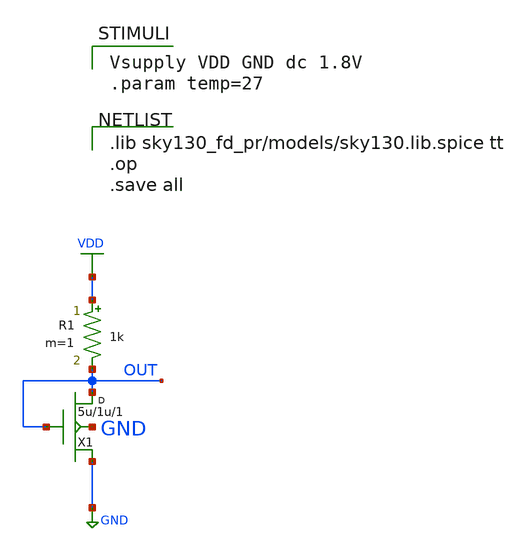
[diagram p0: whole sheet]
** sch_path: tool-test/tooltest.sch
**.subckt tooltest
X1 OUT OUT GND GND sky130_fd_pr__nfet_01v8 w=5u l=1u m=1
R1 VDD OUT 1k m=1
**** begin user architecture code

.lib sky130_fd_pr/models/sky130.lib.spice tt
.op
.save all


Vsupply VDD GND dc 1.8V
.param temp=27

**** end user architecture code
**.ends
.GLOBAL GND
.GLOBAL VDD
.end
